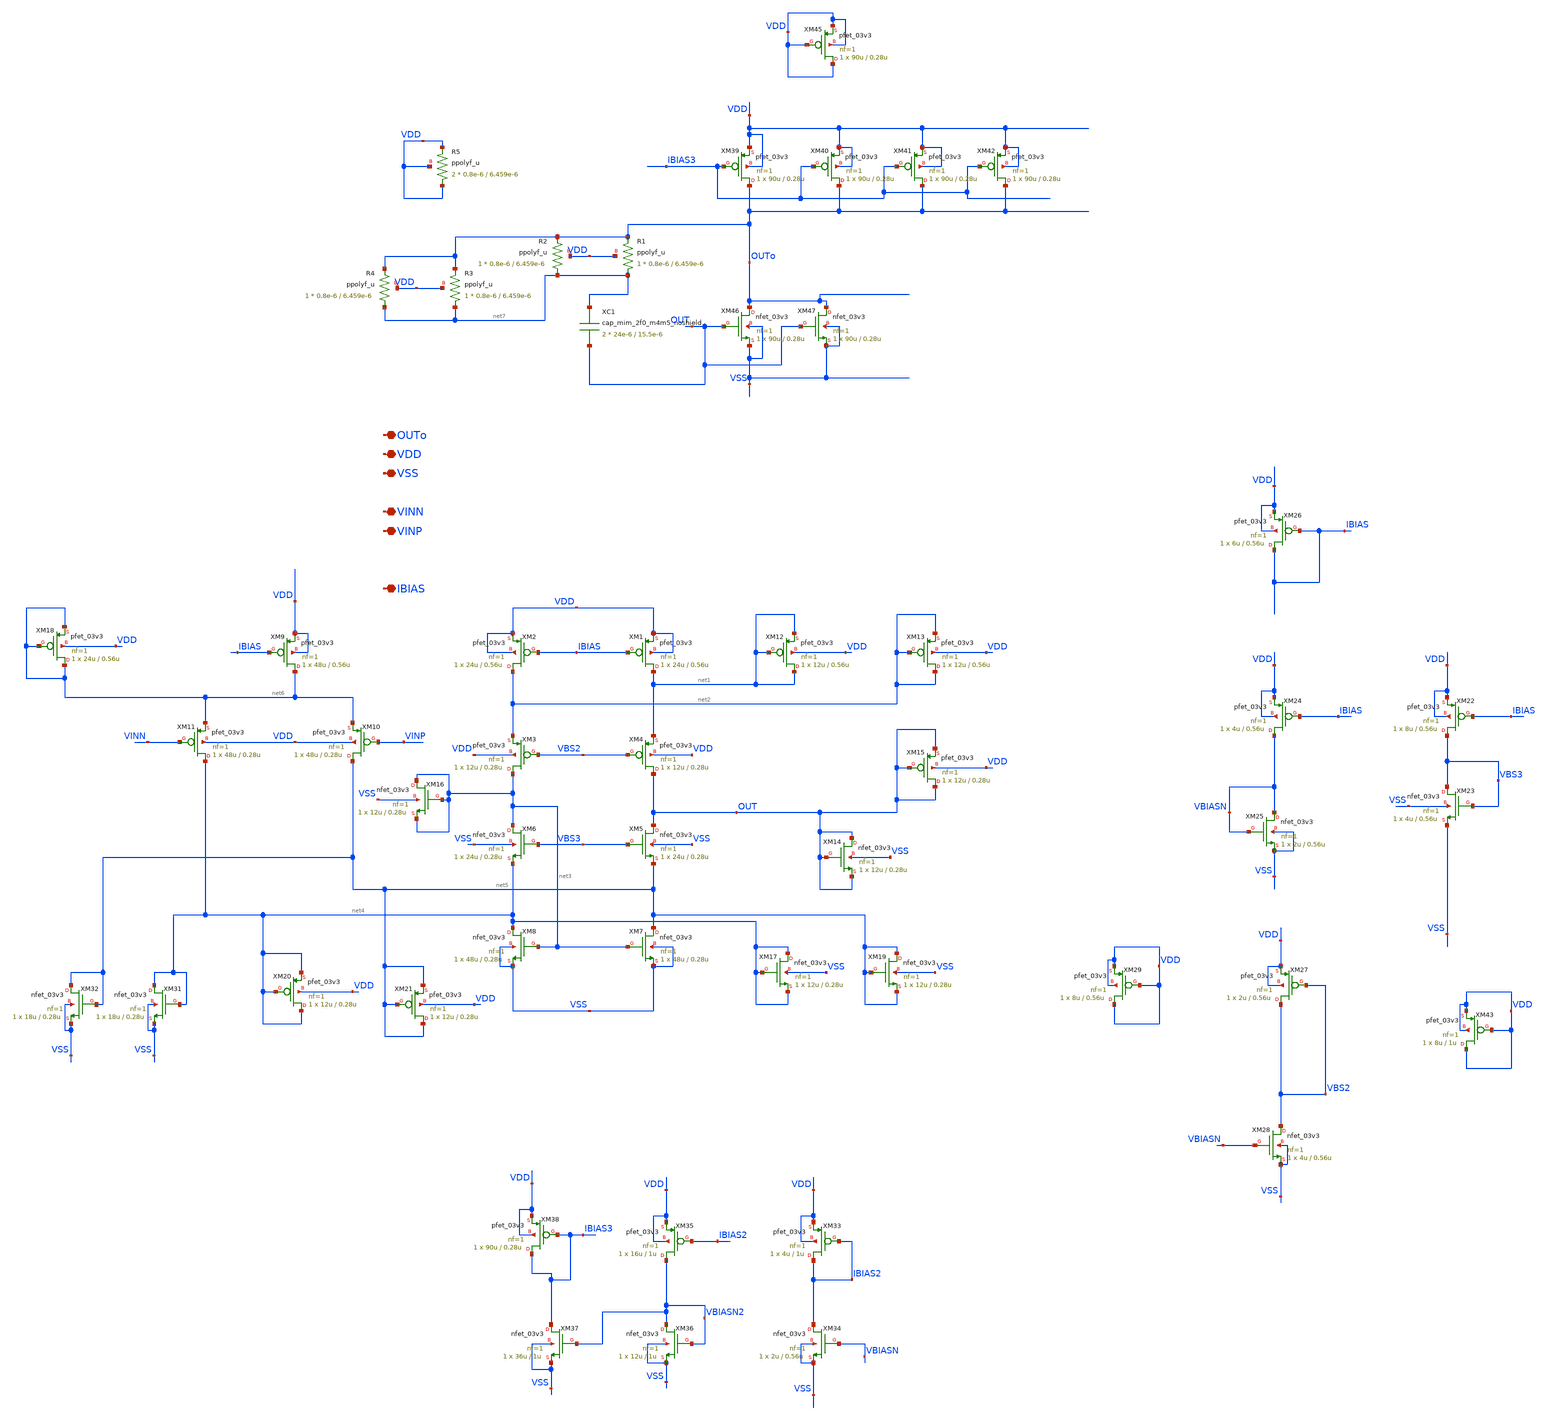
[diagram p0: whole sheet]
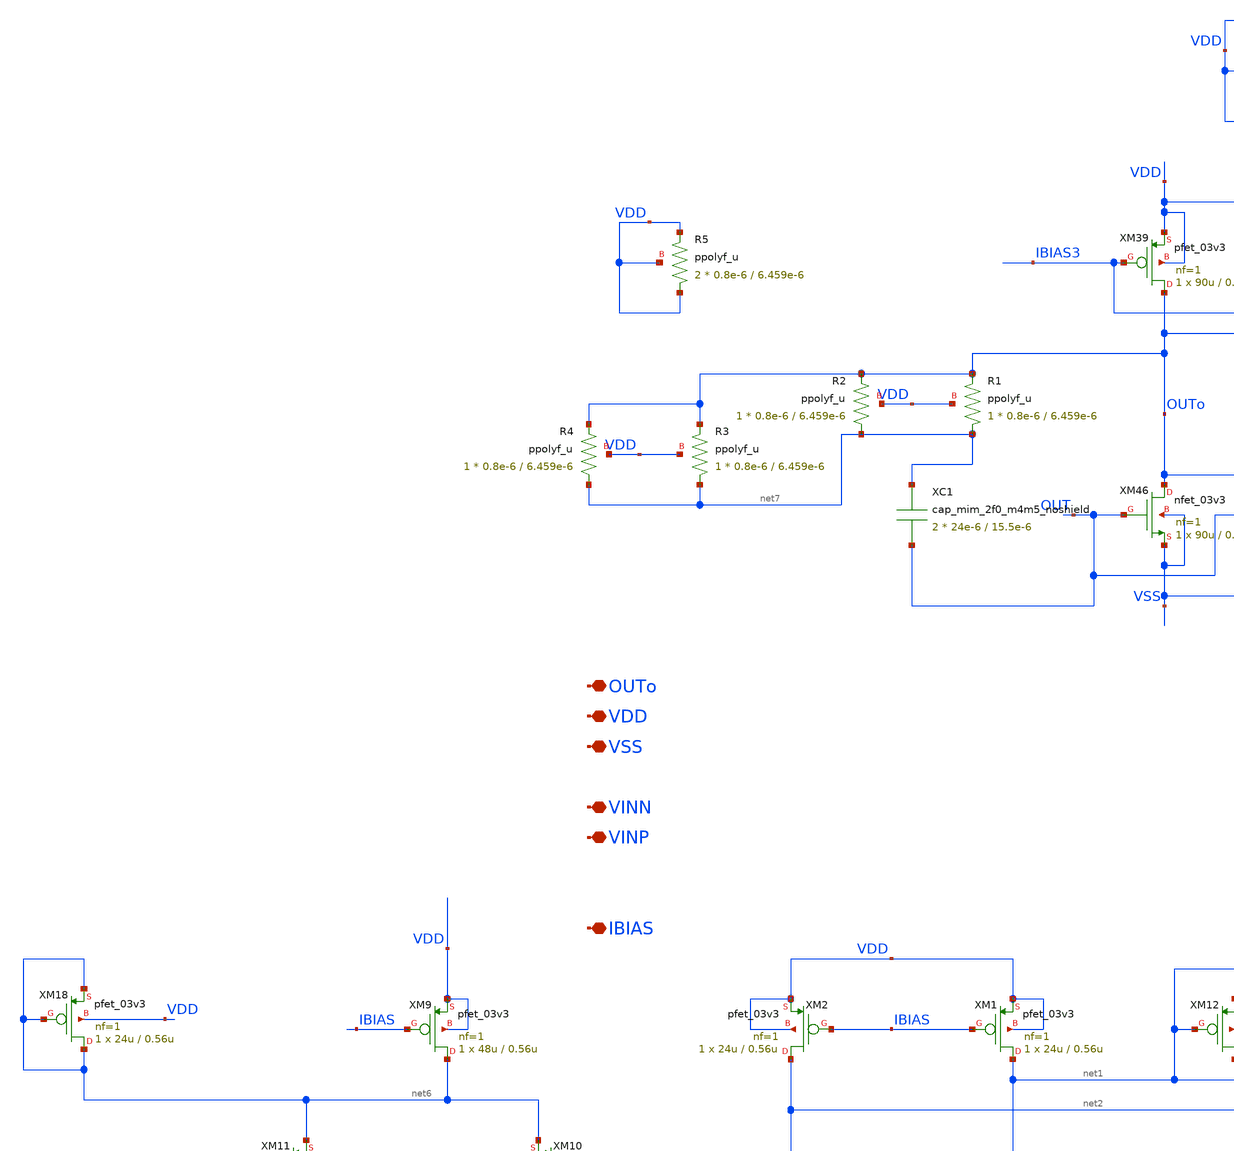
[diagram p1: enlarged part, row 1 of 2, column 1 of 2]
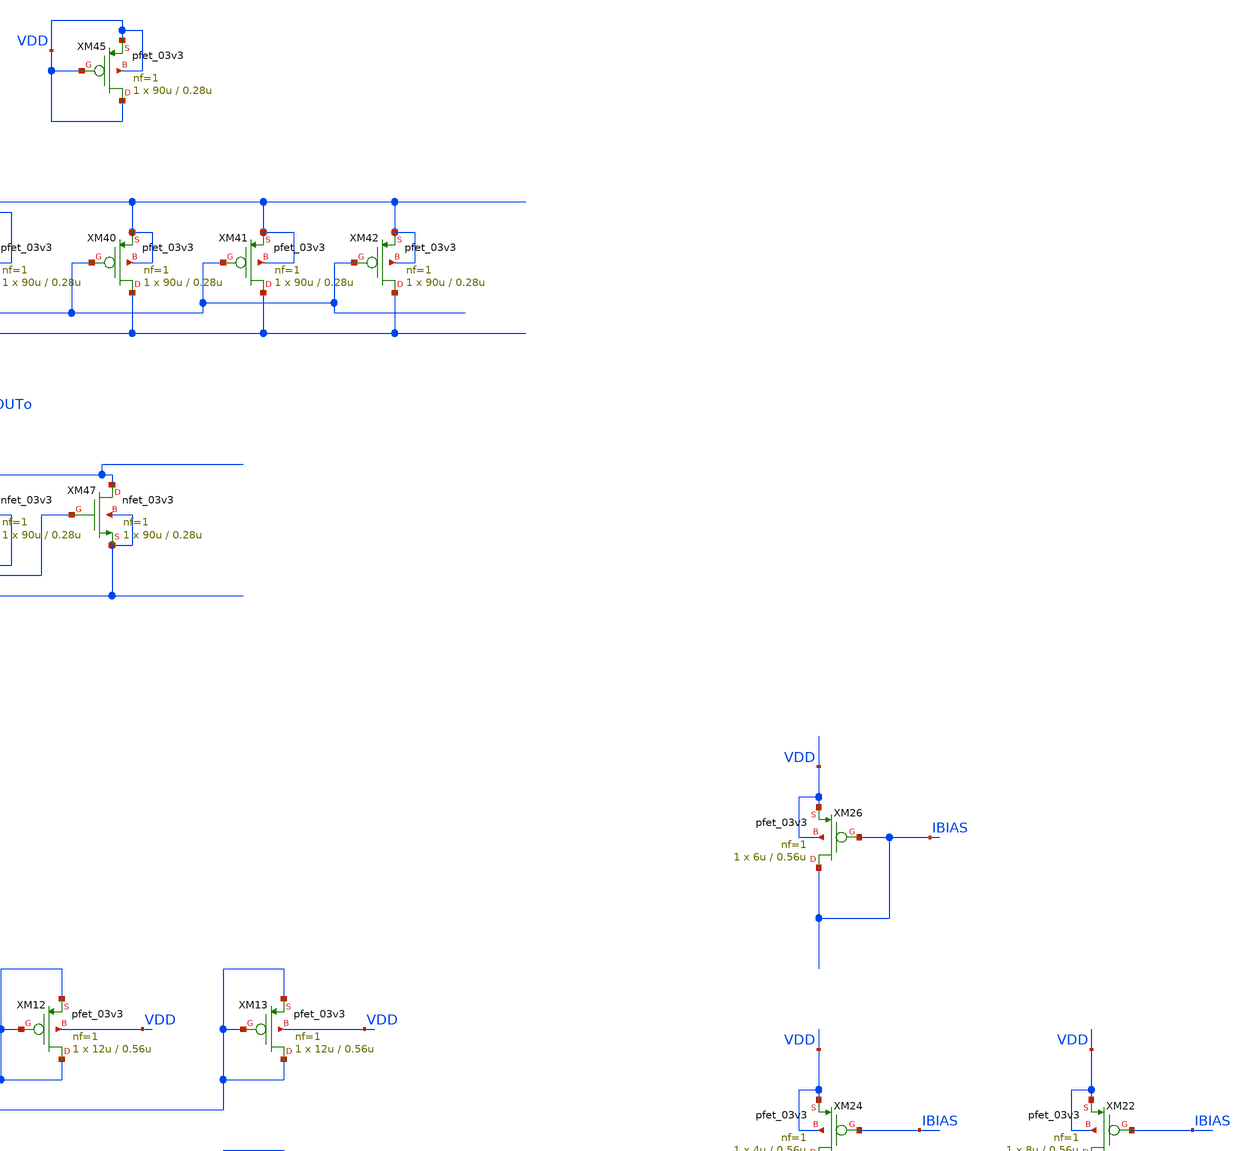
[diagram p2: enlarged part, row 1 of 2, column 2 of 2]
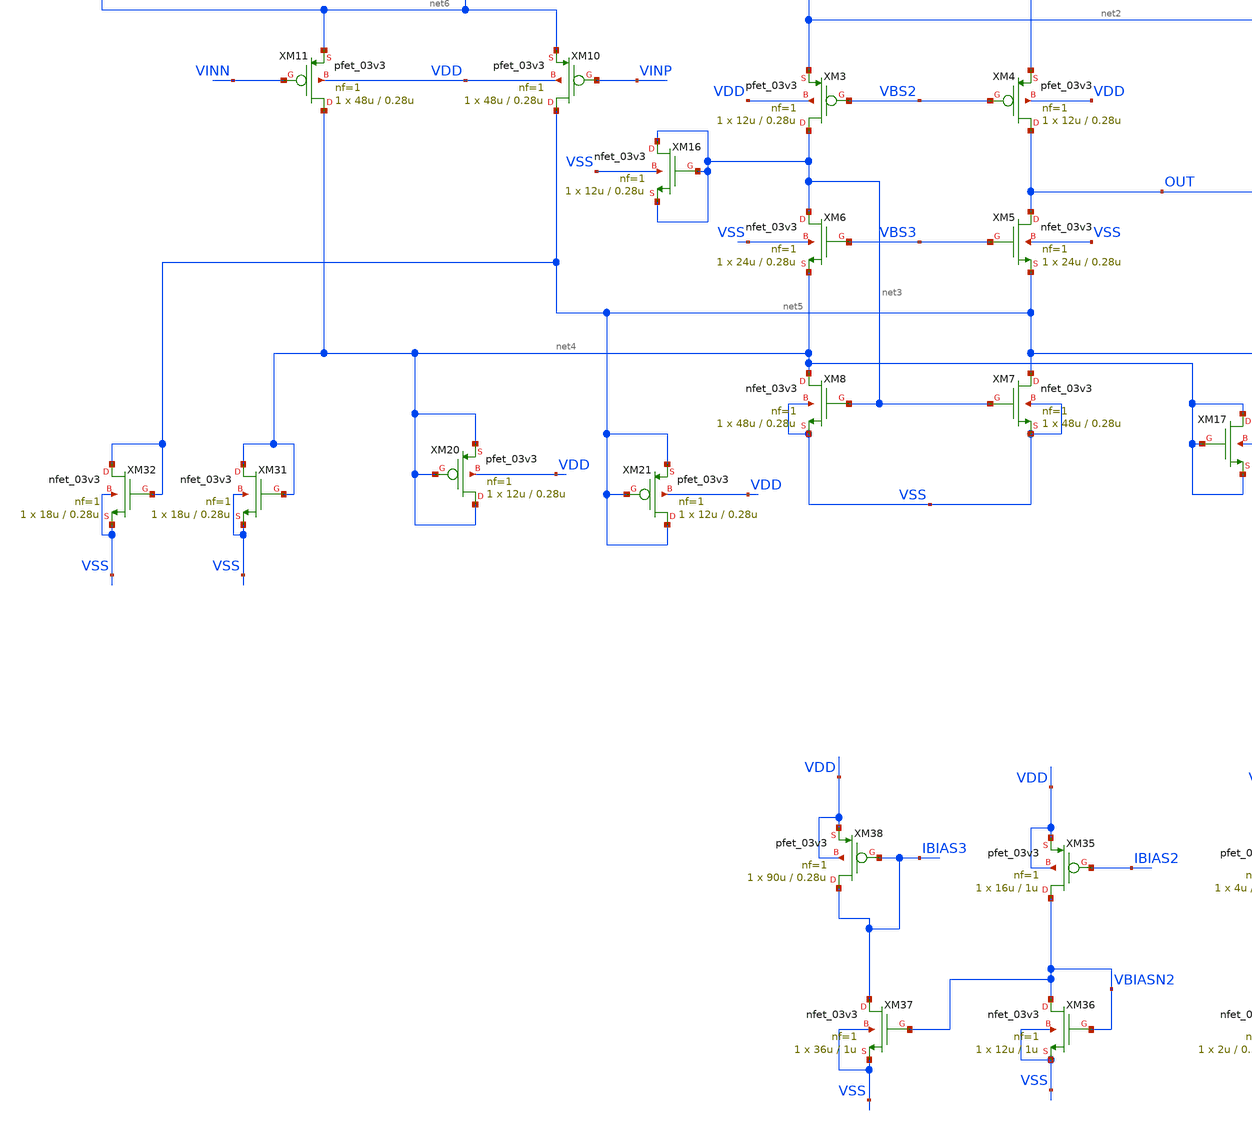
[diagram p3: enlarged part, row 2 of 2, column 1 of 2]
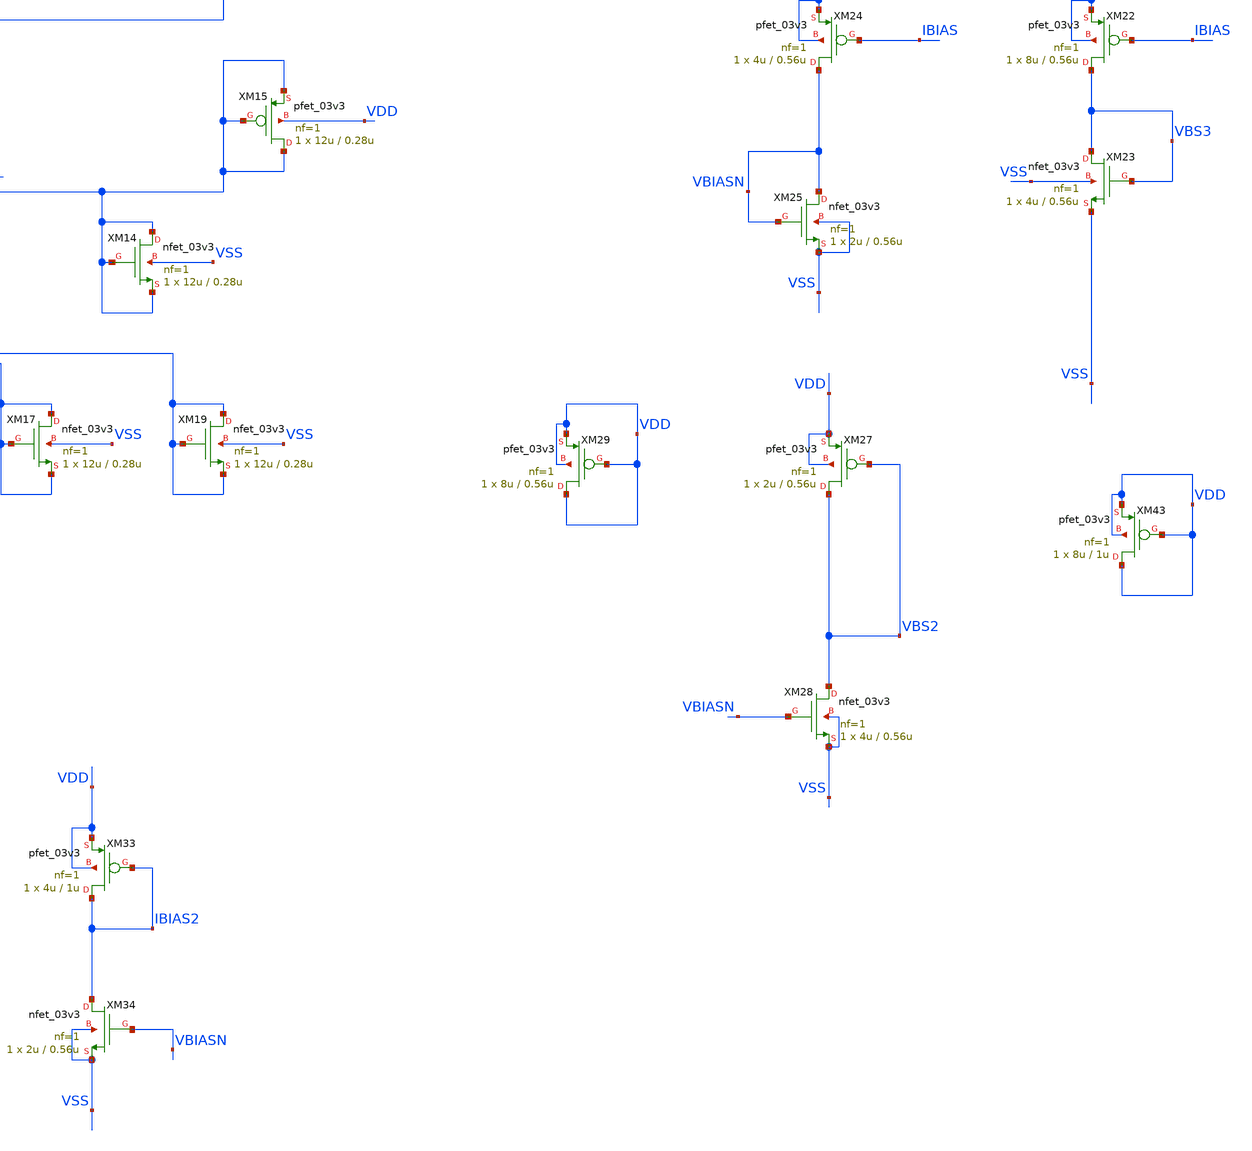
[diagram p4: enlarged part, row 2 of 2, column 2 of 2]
** sch_path: SCOP_INPUT_AND_MUX_PAKISTAN_03/Xschem/Folded_single/folded_single.sch
**.subckt folded_single VDD VSS VINN VINP IBIAS OUTo
*.iopin VDD
*.iopin VSS
*.iopin VINN
*.iopin VINP
*.iopin IBIAS
*.iopin OUTo
XM1 net1 IBIAS VDD VDD pfet_03v3 L=0.56u W=24u nf=1 ad='int((nf+1)/2) * W/nf * 0.18u' as='int((nf+2)/2) * W/nf * 0.18u'
+ pd='2*int((nf+1)/2) * (W/nf + 0.18u)' ps='2*int((nf+2)/2) * (W/nf + 0.18u)' nrd='0.18u / W' nrs='0.18u / W'
+ sa=0 sb=0 sd=0 m=1
XM2 net2 IBIAS VDD VDD pfet_03v3 L=0.56u W=24u nf=1 ad='int((nf+1)/2) * W/nf * 0.18u' as='int((nf+2)/2) * W/nf * 0.18u'
+ pd='2*int((nf+1)/2) * (W/nf + 0.18u)' ps='2*int((nf+2)/2) * (W/nf + 0.18u)' nrd='0.18u / W' nrs='0.18u / W'
+ sa=0 sb=0 sd=0 m=1
XM3 net3 VBS2 net2 VDD pfet_03v3 L=0.28u W=12u nf=1 ad='int((nf+1)/2) * W/nf * 0.18u' as='int((nf+2)/2) * W/nf * 0.18u'
+ pd='2*int((nf+1)/2) * (W/nf + 0.18u)' ps='2*int((nf+2)/2) * (W/nf + 0.18u)' nrd='0.18u / W' nrs='0.18u / W'
+ sa=0 sb=0 sd=0 m=1
XM4 OUT VBS2 net1 VDD pfet_03v3 L=0.28u W=12u nf=1 ad='int((nf+1)/2) * W/nf * 0.18u' as='int((nf+2)/2) * W/nf * 0.18u'
+ pd='2*int((nf+1)/2) * (W/nf + 0.18u)' ps='2*int((nf+2)/2) * (W/nf + 0.18u)' nrd='0.18u / W' nrs='0.18u / W'
+ sa=0 sb=0 sd=0 m=1
XM5 OUT VBS3 net5 VSS nfet_03v3 L=0.28u W=24u nf=1 ad='int((nf+1)/2) * W/nf * 0.18u' as='int((nf+2)/2) * W/nf * 0.18u'
+ pd='2*int((nf+1)/2) * (W/nf + 0.18u)' ps='2*int((nf+2)/2) * (W/nf + 0.18u)' nrd='0.18u / W' nrs='0.18u / W'
+ sa=0 sb=0 sd=0 m=1
XM6 net3 VBS3 net4 VSS nfet_03v3 L=0.28u W=24u nf=1 ad='int((nf+1)/2) * W/nf * 0.18u' as='int((nf+2)/2) * W/nf * 0.18u'
+ pd='2*int((nf+1)/2) * (W/nf + 0.18u)' ps='2*int((nf+2)/2) * (W/nf + 0.18u)' nrd='0.18u / W' nrs='0.18u / W'
+ sa=0 sb=0 sd=0 m=1
XM7 net5 net3 VSS VSS nfet_03v3 L=0.28u W=48u nf=1 ad='int((nf+1)/2) * W/nf * 0.18u' as='int((nf+2)/2) * W/nf * 0.18u'
+ pd='2*int((nf+1)/2) * (W/nf + 0.18u)' ps='2*int((nf+2)/2) * (W/nf + 0.18u)' nrd='0.18u / W' nrs='0.18u / W'
+ sa=0 sb=0 sd=0 m=1
XM8 net4 net3 VSS VSS nfet_03v3 L=0.28u W=48u nf=1 ad='int((nf+1)/2) * W/nf * 0.18u' as='int((nf+2)/2) * W/nf * 0.18u'
+ pd='2*int((nf+1)/2) * (W/nf + 0.18u)' ps='2*int((nf+2)/2) * (W/nf + 0.18u)' nrd='0.18u / W' nrs='0.18u / W'
+ sa=0 sb=0 sd=0 m=1
XM9 net6 IBIAS VDD VDD pfet_03v3 L=0.56u W=48u nf=1 ad='int((nf+1)/2) * W/nf * 0.18u' as='int((nf+2)/2) * W/nf * 0.18u'
+ pd='2*int((nf+1)/2) * (W/nf + 0.18u)' ps='2*int((nf+2)/2) * (W/nf + 0.18u)' nrd='0.18u / W' nrs='0.18u / W'
+ sa=0 sb=0 sd=0 m=1
XM10 net5 VINP net6 VDD pfet_03v3 L=0.28u W=48u nf=1 ad='int((nf+1)/2) * W/nf * 0.18u' as='int((nf+2)/2) * W/nf * 0.18u'
+ pd='2*int((nf+1)/2) * (W/nf + 0.18u)' ps='2*int((nf+2)/2) * (W/nf + 0.18u)' nrd='0.18u / W' nrs='0.18u / W'
+ sa=0 sb=0 sd=0 m=1
XM11 net4 VINN net6 VDD pfet_03v3 L=0.28u W=48u nf=1 ad='int((nf+1)/2) * W/nf * 0.18u' as='int((nf+2)/2) * W/nf * 0.18u'
+ pd='2*int((nf+1)/2) * (W/nf + 0.18u)' ps='2*int((nf+2)/2) * (W/nf + 0.18u)' nrd='0.18u / W' nrs='0.18u / W'
+ sa=0 sb=0 sd=0 m=1
XM12 net1 net1 net1 VDD pfet_03v3 L=0.56u W=12u nf=1 ad='int((nf+1)/2) * W/nf * 0.18u' as='int((nf+2)/2) * W/nf * 0.18u'
+ pd='2*int((nf+1)/2) * (W/nf + 0.18u)' ps='2*int((nf+2)/2) * (W/nf + 0.18u)' nrd='0.18u / W' nrs='0.18u / W'
+ sa=0 sb=0 sd=0 m=1
XM13 net2 net2 net2 VDD pfet_03v3 L=0.56u W=12u nf=1 ad='int((nf+1)/2) * W/nf * 0.18u' as='int((nf+2)/2) * W/nf * 0.18u'
+ pd='2*int((nf+1)/2) * (W/nf + 0.18u)' ps='2*int((nf+2)/2) * (W/nf + 0.18u)' nrd='0.18u / W' nrs='0.18u / W'
+ sa=0 sb=0 sd=0 m=1
XM15 OUT OUT OUT VDD pfet_03v3 L=0.28u W=12u nf=1 ad='int((nf+1)/2) * W/nf * 0.18u' as='int((nf+2)/2) * W/nf * 0.18u'
+ pd='2*int((nf+1)/2) * (W/nf + 0.18u)' ps='2*int((nf+2)/2) * (W/nf + 0.18u)' nrd='0.18u / W' nrs='0.18u / W'
+ sa=0 sb=0 sd=0 m=1
XM18 net6 net6 net6 VDD pfet_03v3 L=0.56u W=24u nf=1 ad='int((nf+1)/2) * W/nf * 0.18u' as='int((nf+2)/2) * W/nf * 0.18u'
+ pd='2*int((nf+1)/2) * (W/nf + 0.18u)' ps='2*int((nf+2)/2) * (W/nf + 0.18u)' nrd='0.18u / W' nrs='0.18u / W'
+ sa=0 sb=0 sd=0 m=1
XM14 OUT OUT OUT VSS nfet_03v3 L=0.28u W=12u nf=1 ad='int((nf+1)/2) * W/nf * 0.18u' as='int((nf+2)/2) * W/nf * 0.18u'
+ pd='2*int((nf+1)/2) * (W/nf + 0.18u)' ps='2*int((nf+2)/2) * (W/nf + 0.18u)' nrd='0.18u / W' nrs='0.18u / W'
+ sa=0 sb=0 sd=0 m=1
XM16 net3 net3 net3 VSS nfet_03v3 L=0.28u W=12u nf=1 ad='int((nf+1)/2) * W/nf * 0.18u' as='int((nf+2)/2) * W/nf * 0.18u'
+ pd='2*int((nf+1)/2) * (W/nf + 0.18u)' ps='2*int((nf+2)/2) * (W/nf + 0.18u)' nrd='0.18u / W' nrs='0.18u / W'
+ sa=0 sb=0 sd=0 m=1
XM17 net4 net4 net4 VSS nfet_03v3 L=0.28u W=12u nf=1 ad='int((nf+1)/2) * W/nf * 0.18u' as='int((nf+2)/2) * W/nf * 0.18u'
+ pd='2*int((nf+1)/2) * (W/nf + 0.18u)' ps='2*int((nf+2)/2) * (W/nf + 0.18u)' nrd='0.18u / W' nrs='0.18u / W'
+ sa=0 sb=0 sd=0 m=1
XM19 net5 net5 net5 VSS nfet_03v3 L=0.28u W=12u nf=1 ad='int((nf+1)/2) * W/nf * 0.18u' as='int((nf+2)/2) * W/nf * 0.18u'
+ pd='2*int((nf+1)/2) * (W/nf + 0.18u)' ps='2*int((nf+2)/2) * (W/nf + 0.18u)' nrd='0.18u / W' nrs='0.18u / W'
+ sa=0 sb=0 sd=0 m=1
XM20 net4 net4 net4 VDD pfet_03v3 L=0.28u W=12u nf=1 ad='int((nf+1)/2) * W/nf * 0.18u' as='int((nf+2)/2) * W/nf * 0.18u'
+ pd='2*int((nf+1)/2) * (W/nf + 0.18u)' ps='2*int((nf+2)/2) * (W/nf + 0.18u)' nrd='0.18u / W' nrs='0.18u / W'
+ sa=0 sb=0 sd=0 m=1
XM21 net5 net5 net5 VDD pfet_03v3 L=0.28u W=12u nf=1 ad='int((nf+1)/2) * W/nf * 0.18u' as='int((nf+2)/2) * W/nf * 0.18u'
+ pd='2*int((nf+1)/2) * (W/nf + 0.18u)' ps='2*int((nf+2)/2) * (W/nf + 0.18u)' nrd='0.18u / W' nrs='0.18u / W'
+ sa=0 sb=0 sd=0 m=1
XM22 VBS3 IBIAS VDD VDD pfet_03v3 L=0.56u W=8u nf=1 ad='int((nf+1)/2) * W/nf * 0.18u' as='int((nf+2)/2) * W/nf * 0.18u'
+ pd='2*int((nf+1)/2) * (W/nf + 0.18u)' ps='2*int((nf+2)/2) * (W/nf + 0.18u)' nrd='0.18u / W' nrs='0.18u / W'
+ sa=0 sb=0 sd=0 m=1
XM23 VBS3 VBS3 VSS VSS nfet_03v3 L=0.56u W=4u nf=1 ad='int((nf+1)/2) * W/nf * 0.18u' as='int((nf+2)/2) * W/nf * 0.18u'
+ pd='2*int((nf+1)/2) * (W/nf + 0.18u)' ps='2*int((nf+2)/2) * (W/nf + 0.18u)' nrd='0.18u / W' nrs='0.18u / W'
+ sa=0 sb=0 sd=0 m=1
XM24 VBIASN IBIAS VDD VDD pfet_03v3 L=0.56u W=4u nf=1 ad='int((nf+1)/2) * W/nf * 0.18u' as='int((nf+2)/2) * W/nf * 0.18u'
+ pd='2*int((nf+1)/2) * (W/nf + 0.18u)' ps='2*int((nf+2)/2) * (W/nf + 0.18u)' nrd='0.18u / W' nrs='0.18u / W'
+ sa=0 sb=0 sd=0 m=1
XM25 VBIASN VBIASN VSS VSS nfet_03v3 L=0.56u W=2u nf=1 ad='int((nf+1)/2) * W/nf * 0.18u' as='int((nf+2)/2) * W/nf * 0.18u'
+ pd='2*int((nf+1)/2) * (W/nf + 0.18u)' ps='2*int((nf+2)/2) * (W/nf + 0.18u)' nrd='0.18u / W' nrs='0.18u / W'
+ sa=0 sb=0 sd=0 m=1
XM26 IBIAS IBIAS VDD VDD pfet_03v3 L=0.56u W=6u nf=1 ad='int((nf+1)/2) * W/nf * 0.18u' as='int((nf+2)/2) * W/nf * 0.18u'
+ pd='2*int((nf+1)/2) * (W/nf + 0.18u)' ps='2*int((nf+2)/2) * (W/nf + 0.18u)' nrd='0.18u / W' nrs='0.18u / W'
+ sa=0 sb=0 sd=0 m=1
XM27 VBS2 VBS2 VDD VDD pfet_03v3 L=0.56u W=2u nf=1 ad='int((nf+1)/2) * W/nf * 0.18u' as='int((nf+2)/2) * W/nf * 0.18u'
+ pd='2*int((nf+1)/2) * (W/nf + 0.18u)' ps='2*int((nf+2)/2) * (W/nf + 0.18u)' nrd='0.18u / W' nrs='0.18u / W'
+ sa=0 sb=0 sd=0 m=1
XM28 VBS2 VBIASN VSS VSS nfet_03v3 L=0.56u W=4u nf=1 ad='int((nf+1)/2) * W/nf * 0.18u' as='int((nf+2)/2) * W/nf * 0.18u'
+ pd='2*int((nf+1)/2) * (W/nf + 0.18u)' ps='2*int((nf+2)/2) * (W/nf + 0.18u)' nrd='0.18u / W' nrs='0.18u / W'
+ sa=0 sb=0 sd=0 m=1
XM29 VDD VDD VDD VDD pfet_03v3 L=0.56u W=8u nf=1 ad='int((nf+1)/2) * W/nf * 0.18u' as='int((nf+2)/2) * W/nf * 0.18u'
+ pd='2*int((nf+1)/2) * (W/nf + 0.18u)' ps='2*int((nf+2)/2) * (W/nf + 0.18u)' nrd='0.18u / W' nrs='0.18u / W'
+ sa=0 sb=0 sd=0 m=1
XM31 net4 net4 VSS VSS nfet_03v3 L=0.28u W=18u nf=1 ad='int((nf+1)/2) * W/nf * 0.18u' as='int((nf+2)/2) * W/nf * 0.18u'
+ pd='2*int((nf+1)/2) * (W/nf + 0.18u)' ps='2*int((nf+2)/2) * (W/nf + 0.18u)' nrd='0.18u / W' nrs='0.18u / W'
+ sa=0 sb=0 sd=0 m=1
XM32 net5 net5 VSS VSS nfet_03v3 L=0.28u W=18u nf=1 ad='int((nf+1)/2) * W/nf * 0.18u' as='int((nf+2)/2) * W/nf * 0.18u'
+ pd='2*int((nf+1)/2) * (W/nf + 0.18u)' ps='2*int((nf+2)/2) * (W/nf + 0.18u)' nrd='0.18u / W' nrs='0.18u / W'
+ sa=0 sb=0 sd=0 m=1
XM33 IBIAS2 IBIAS2 VDD VDD pfet_03v3 L=1u W=4u nf=1 ad='int((nf+1)/2) * W/nf * 0.18u' as='int((nf+2)/2) * W/nf * 0.18u'
+ pd='2*int((nf+1)/2) * (W/nf + 0.18u)' ps='2*int((nf+2)/2) * (W/nf + 0.18u)' nrd='0.18u / W' nrs='0.18u / W'
+ sa=0 sb=0 sd=0 m=1
XM34 IBIAS2 VBIASN VSS VSS nfet_03v3 L=0.56u W=2u nf=1 ad='int((nf+1)/2) * W/nf * 0.18u' as='int((nf+2)/2) * W/nf * 0.18u'
+ pd='2*int((nf+1)/2) * (W/nf + 0.18u)' ps='2*int((nf+2)/2) * (W/nf + 0.18u)' nrd='0.18u / W' nrs='0.18u / W'
+ sa=0 sb=0 sd=0 m=1
XM35 VBIASN2 IBIAS2 VDD VDD pfet_03v3 L=1u W=16u nf=1 ad='int((nf+1)/2) * W/nf * 0.18u' as='int((nf+2)/2) * W/nf * 0.18u'
+ pd='2*int((nf+1)/2) * (W/nf + 0.18u)' ps='2*int((nf+2)/2) * (W/nf + 0.18u)' nrd='0.18u / W' nrs='0.18u / W'
+ sa=0 sb=0 sd=0 m=1
XM36 VBIASN2 VBIASN2 VSS VSS nfet_03v3 L=1u W=12u nf=1 ad='int((nf+1)/2) * W/nf * 0.18u' as='int((nf+2)/2) * W/nf * 0.18u'
+ pd='2*int((nf+1)/2) * (W/nf + 0.18u)' ps='2*int((nf+2)/2) * (W/nf + 0.18u)' nrd='0.18u / W' nrs='0.18u / W'
+ sa=0 sb=0 sd=0 m=1
XM37 IBIAS3 VBIASN2 VSS VSS nfet_03v3 L=1u W=36u nf=1 ad='int((nf+1)/2) * W/nf * 0.18u' as='int((nf+2)/2) * W/nf * 0.18u'
+ pd='2*int((nf+1)/2) * (W/nf + 0.18u)' ps='2*int((nf+2)/2) * (W/nf + 0.18u)' nrd='0.18u / W' nrs='0.18u / W'
+ sa=0 sb=0 sd=0 m=1
XM38 IBIAS3 IBIAS3 VDD VDD pfet_03v3 L=0.28u W=90u nf=1 ad='int((nf+1)/2) * W/nf * 0.18u' as='int((nf+2)/2) * W/nf * 0.18u'
+ pd='2*int((nf+1)/2) * (W/nf + 0.18u)' ps='2*int((nf+2)/2) * (W/nf + 0.18u)' nrd='0.18u / W' nrs='0.18u / W'
+ sa=0 sb=0 sd=0 m=1
XM39 OUTo IBIAS3 VDD VDD pfet_03v3 L=0.28u W=90u nf=1 ad='int((nf+1)/2) * W/nf * 0.18u' as='int((nf+2)/2) * W/nf * 0.18u'
+ pd='2*int((nf+1)/2) * (W/nf + 0.18u)' ps='2*int((nf+2)/2) * (W/nf + 0.18u)' nrd='0.18u / W' nrs='0.18u / W'
+ sa=0 sb=0 sd=0 m=1
XM40 OUTo IBIAS3 VDD VDD pfet_03v3 L=0.28u W=90u nf=1 ad='int((nf+1)/2) * W/nf * 0.18u' as='int((nf+2)/2) * W/nf * 0.18u'
+ pd='2*int((nf+1)/2) * (W/nf + 0.18u)' ps='2*int((nf+2)/2) * (W/nf + 0.18u)' nrd='0.18u / W' nrs='0.18u / W'
+ sa=0 sb=0 sd=0 m=1
XM41 OUTo IBIAS3 VDD VDD pfet_03v3 L=0.28u W=90u nf=1 ad='int((nf+1)/2) * W/nf * 0.18u' as='int((nf+2)/2) * W/nf * 0.18u'
+ pd='2*int((nf+1)/2) * (W/nf + 0.18u)' ps='2*int((nf+2)/2) * (W/nf + 0.18u)' nrd='0.18u / W' nrs='0.18u / W'
+ sa=0 sb=0 sd=0 m=1
XM42 OUTo IBIAS3 VDD VDD pfet_03v3 L=0.28u W=90u nf=1 ad='int((nf+1)/2) * W/nf * 0.18u' as='int((nf+2)/2) * W/nf * 0.18u'
+ pd='2*int((nf+1)/2) * (W/nf + 0.18u)' ps='2*int((nf+2)/2) * (W/nf + 0.18u)' nrd='0.18u / W' nrs='0.18u / W'
+ sa=0 sb=0 sd=0 m=1
XM43 VDD VDD VDD VDD pfet_03v3 L=1u W=8u nf=1 ad='int((nf+1)/2) * W/nf * 0.18u' as='int((nf+2)/2) * W/nf * 0.18u'
+ pd='2*int((nf+1)/2) * (W/nf + 0.18u)' ps='2*int((nf+2)/2) * (W/nf + 0.18u)' nrd='0.18u / W' nrs='0.18u / W'
+ sa=0 sb=0 sd=0 m=1
XM45 VDD VDD VDD VDD pfet_03v3 L=0.28u W=90u nf=1 ad='int((nf+1)/2) * W/nf * 0.18u' as='int((nf+2)/2) * W/nf * 0.18u'
+ pd='2*int((nf+1)/2) * (W/nf + 0.18u)' ps='2*int((nf+2)/2) * (W/nf + 0.18u)' nrd='0.18u / W' nrs='0.18u / W'
+ sa=0 sb=0 sd=0 m=1
XM46 OUTo OUT VSS VSS nfet_03v3 L=0.28u W=90u nf=1 ad='int((nf+1)/2) * W/nf * 0.18u' as='int((nf+2)/2) * W/nf * 0.18u'
+ pd='2*int((nf+1)/2) * (W/nf + 0.18u)' ps='2*int((nf+2)/2) * (W/nf + 0.18u)' nrd='0.18u / W' nrs='0.18u / W'
+ sa=0 sb=0 sd=0 m=1
XM47 OUTo OUT VSS VSS nfet_03v3 L=0.28u W=90u nf=1 ad='int((nf+1)/2) * W/nf * 0.18u' as='int((nf+2)/2) * W/nf * 0.18u'
+ pd='2*int((nf+1)/2) * (W/nf + 0.18u)' ps='2*int((nf+2)/2) * (W/nf + 0.18u)' nrd='0.18u / W' nrs='0.18u / W'
+ sa=0 sb=0 sd=0 m=1
XR1 net7 OUTo VDD ppolyf_u r_width=0.8e-6 r_length=6.459e-6 m=1
XC1 net7 OUT cap_mim_2f0_m4m5_noshield c_width=24e-6 c_length=15.5e-6 m=2
XR2 net7 OUTo VDD ppolyf_u r_width=0.8e-6 r_length=6.459e-6 m=1
XR3 net7 OUTo VDD ppolyf_u r_width=0.8e-6 r_length=6.459e-6 m=1
XR4 net7 OUTo VDD ppolyf_u r_width=0.8e-6 r_length=6.459e-6 m=1
XR5 VDD VDD VDD ppolyf_u r_width=0.8e-6 r_length=6.459e-6 m=2
**.ends
.end
